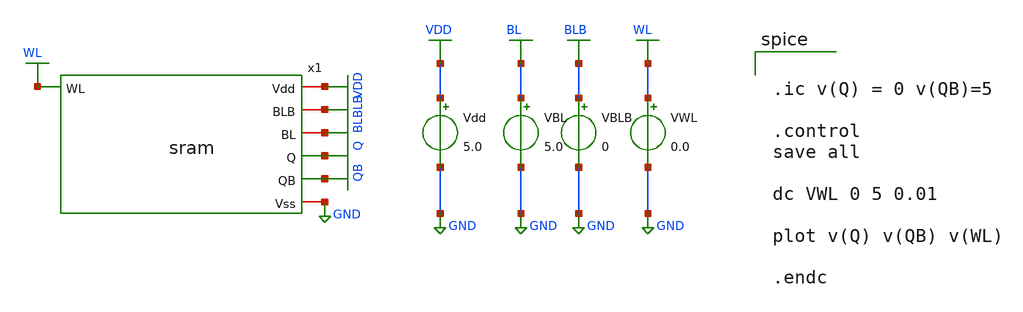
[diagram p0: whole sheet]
** sch_path: sram_tb_dc_write.sch
**.subckt sram_tb_dc_write
Vdd VDD GND 5.0
VBL BL GND 5.0
VBLB BLB GND 0
VWL WL GND 0.0
x1 WL VDD BLB BL Q QB GND sram
**** begin user architecture code
 .include $::LIB/ip62_models


.ic v(Q) = 0 v(QB)=5

.control
save all

dc VWL 0 5 0.01

plot v(Q) v(QB) v(WL)

.endc



**** end user architecture code
**.ends

* expanding   symbol:  sram.sym # of pins=7
** sym_path: sram.sym
** sch_path: sram.sch
.subckt sram WL Vdd BLB BL Q QB Vss
*.iopin Vdd
*.iopin Vss
*.iopin BLB
*.iopin BL
*.ipin WL
*.opin Q
*.opin QB
XXM1 Q QB Vss Vss NMOS w=3.4u l=1u nrd=0 nrs=0 m=1
XXM2 Q QB Vdd Vdd PMOS w=3.4u l=1u nrd=0 nrs=0 m=1
XXM3 QB Q Vss Vss NMOS w=3.4u l=1u nrd=0 nrs=0 m=1
XXM4 QB Q Vdd Vdd PMOS w=3.4u l=1u nrd=0 nrs=0 m=1
XXM7 Q WL BL Vss NMOS w=3.4u l=1u nrd=0 nrs=0 m=1
XXM6 QB WL BLB Vss NMOS w=3.4u l=1u nrd=0 nrs=0 m=1
.ends

.GLOBAL VDD
.GLOBAL GND
.GLOBAL QB
.GLOBAL Q
.GLOBAL BLB
.GLOBAL BL
.GLOBAL WL
.end
